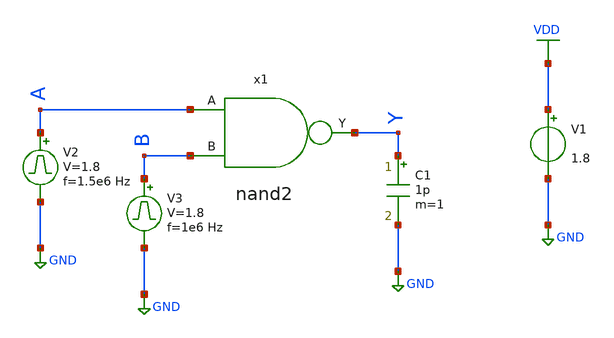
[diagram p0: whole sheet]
** sch_path: library/xschem/nand2_tb.sch
**.subckt nand2_tb
V1 VDD GND 1.8
V2 A GND pulse 0 1.8 '0.495/ 1.5e6 ' '0.01/1.5e6 ' '0.01/1.5e6 ' '0.49/1.5e6 ' '1/1.5e6 '
C1 Y GND 1p m=1
x1 A Y B nand2
V3 B GND pulse 0 1.8 '0.495/ 1e6 ' '0.01/1e6 ' '0.01/1e6 ' '0.49/1e6 ' '1/1e6 '
**** begin user architecture code


.control
save all
tran 1n 2u
plot V(A) V(B) V(Y)
.endc


** opencircuitdesign pdks install
.lib $::SKYWATER_MODELS/sky130.lib.spice tt


**** end user architecture code
**.ends

* expanding   symbol:  nand2.sym # of pins=3
** sym_path: library/xschem/nand2.sym
** sch_path: library/xschem/nand2.sch
.subckt nand2 A Y B
*.opin Y
*.ipin A
*.ipin B
XM1 Y B net1 GND sky130_fd_pr__nfet_01v8 L=0.15 W=1 nf=1 ad='int((nf+1)/2) * W/nf * 0.29' as='int((nf+2)/2) * W/nf * 0.29'
+ pd='2*int((nf+1)/2) * (W/nf + 0.29)' ps='2*int((nf+2)/2) * (W/nf + 0.29)' nrd='0.29 / W' nrs='0.29 / W'
+ sa=0 sb=0 sd=0 mult=1 m=1
XM2 Y B VDD VDD sky130_fd_pr__pfet_01v8 L=0.15 W=1 nf=1 ad='int((nf+1)/2) * W/nf * 0.29' as='int((nf+2)/2) * W/nf * 0.29'
+ pd='2*int((nf+1)/2) * (W/nf + 0.29)' ps='2*int((nf+2)/2) * (W/nf + 0.29)' nrd='0.29 / W' nrs='0.29 / W'
+ sa=0 sb=0 sd=0 mult=1 m=1
XM3 Y A VDD VDD sky130_fd_pr__pfet_01v8 L=0.15 W=1 nf=1 ad='int((nf+1)/2) * W/nf * 0.29' as='int((nf+2)/2) * W/nf * 0.29'
+ pd='2*int((nf+1)/2) * (W/nf + 0.29)' ps='2*int((nf+2)/2) * (W/nf + 0.29)' nrd='0.29 / W' nrs='0.29 / W'
+ sa=0 sb=0 sd=0 mult=1 m=1
XM4 net1 A GND GND sky130_fd_pr__nfet_01v8 L=0.15 W=1 nf=1 ad='int((nf+1)/2) * W/nf * 0.29' as='int((nf+2)/2) * W/nf * 0.29'
+ pd='2*int((nf+1)/2) * (W/nf + 0.29)' ps='2*int((nf+2)/2) * (W/nf + 0.29)' nrd='0.29 / W' nrs='0.29 / W'
+ sa=0 sb=0 sd=0 mult=1 m=1
.ends

.GLOBAL VDD
.GLOBAL GND
.end
